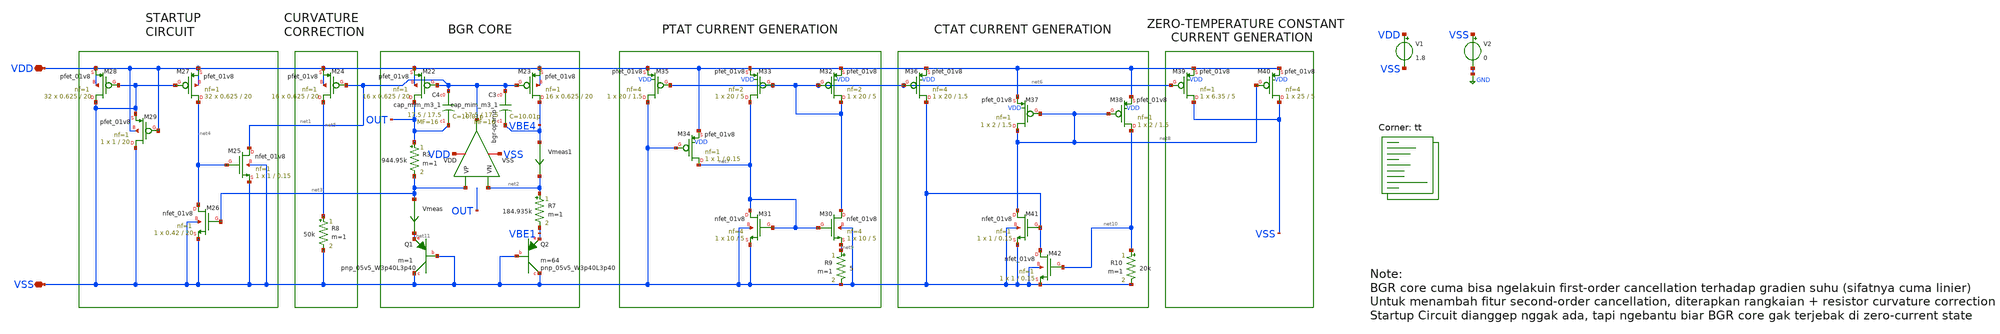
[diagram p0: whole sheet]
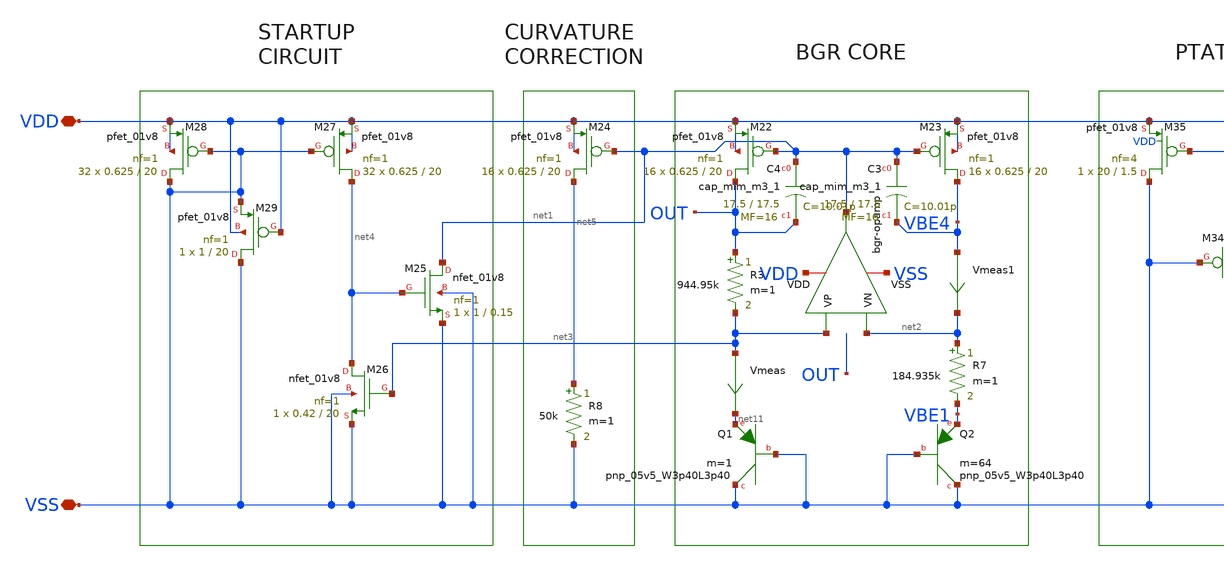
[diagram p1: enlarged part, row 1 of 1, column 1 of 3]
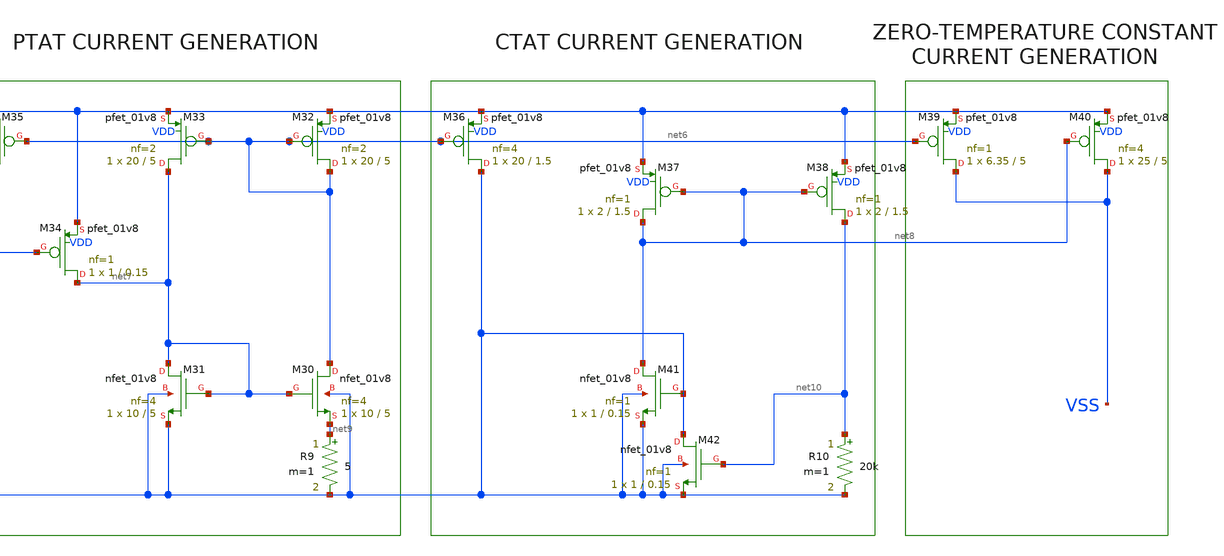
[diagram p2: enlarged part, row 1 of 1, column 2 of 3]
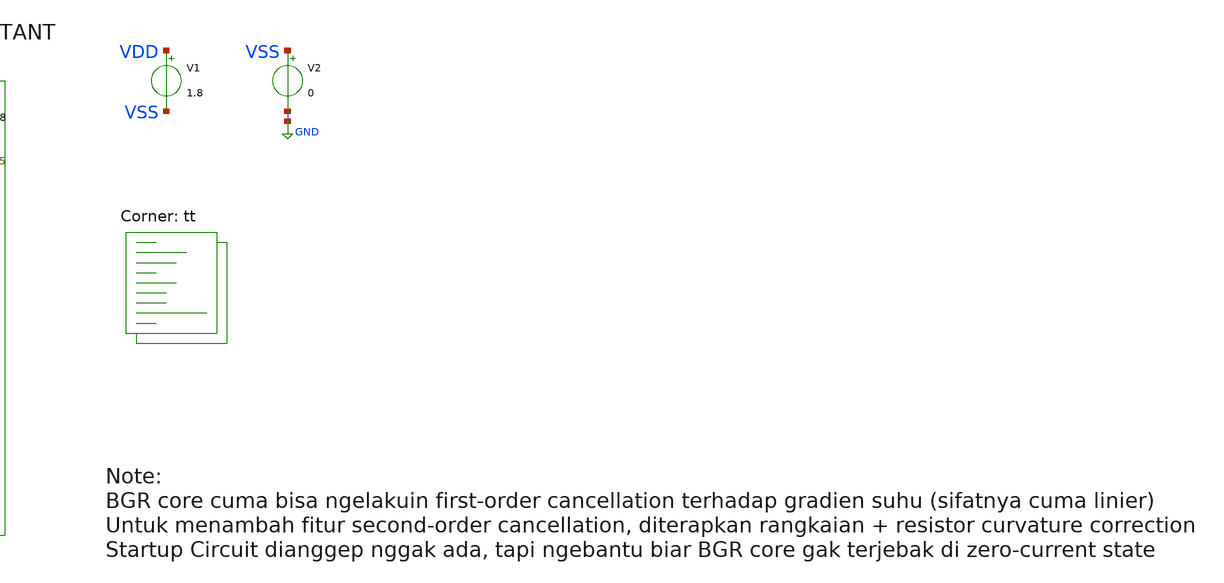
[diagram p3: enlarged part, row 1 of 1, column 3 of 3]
** sch_path: bandgap/bgr2.sch
**.subckt bgr2 VDD VSS
*.iopin VDD
*.iopin VSS
V1 VDD VSS 1.8
V2 VSS GND 0
x1 VDD net1 net3 net2 VSS bgr-opamp
XM22 OUT net1 VDD VDD sky130_fd_pr__pfet_01v8 L=20 W=0.625 nf=1 ad='int((nf+1)/2) * W/nf * 0.29' as='int((nf+2)/2) * W/nf * 0.29'
+ pd='2*int((nf+1)/2) * (W/nf + 0.29)' ps='2*int((nf+2)/2) * (W/nf + 0.29)' nrd='0.29 / W' nrs='0.29 / W'
+ sa=0 sb=0 sd=0 mult=16 m=16
XM23 VBE4 net1 VDD VDD sky130_fd_pr__pfet_01v8 L=20 W=0.625 nf=1 ad='int((nf+1)/2) * W/nf * 0.29' as='int((nf+2)/2) * W/nf * 0.29'
+ pd='2*int((nf+1)/2) * (W/nf + 0.29)' ps='2*int((nf+2)/2) * (W/nf + 0.29)' nrd='0.29 / W' nrs='0.29 / W'
+ sa=0 sb=0 sd=0 mult=16 m=16
R3 OUT net3 944.95k m=1
R7 net2 VBE1 184.935k m=1
XQ1 VSS VSS net11 sky130_fd_pr__pnp_05v5_W3p40L3p40 m=1
XQ2 VSS VSS VBE1 sky130_fd_pr__pnp_05v5_W3p40L3p40 m=64
XM24 net5 net1 VDD VDD sky130_fd_pr__pfet_01v8 L=20 W=0.625 nf=1 ad='int((nf+1)/2) * W/nf * 0.29' as='int((nf+2)/2) * W/nf * 0.29'
+ pd='2*int((nf+1)/2) * (W/nf + 0.29)' ps='2*int((nf+2)/2) * (W/nf + 0.29)' nrd='0.29 / W' nrs='0.29 / W'
+ sa=0 sb=0 sd=0 mult=16 m=16
XM25 net1 net4 VSS VSS sky130_fd_pr__nfet_01v8 L=0.15 W=1 nf=1 ad='int((nf+1)/2) * W/nf * 0.29' as='int((nf+2)/2) * W/nf * 0.29'
+ pd='2*int((nf+1)/2) * (W/nf + 0.29)' ps='2*int((nf+2)/2) * (W/nf + 0.29)' nrd='0.29 / W' nrs='0.29 / W'
+ sa=0 sb=0 sd=0 mult=1 m=1
XM26 net4 net3 VSS VSS sky130_fd_pr__nfet_01v8 L=20 W=0.42 nf=1 ad='int((nf+1)/2) * W/nf * 0.29' as='int((nf+2)/2) * W/nf * 0.29'
+ pd='2*int((nf+1)/2) * (W/nf + 0.29)' ps='2*int((nf+2)/2) * (W/nf + 0.29)' nrd='0.29 / W' nrs='0.29 / W'
+ sa=0 sb=0 sd=0 mult=1 m=1
XM27 net4 VSS VDD VDD sky130_fd_pr__pfet_01v8 L=20 W=0.625 nf=1 ad='int((nf+1)/2) * W/nf * 0.29' as='int((nf+2)/2) * W/nf * 0.29'
+ pd='2*int((nf+1)/2) * (W/nf + 0.29)' ps='2*int((nf+2)/2) * (W/nf + 0.29)' nrd='0.29 / W' nrs='0.29 / W'
+ sa=0 sb=0 sd=0 mult=32 m=32
XM28 VSS VSS VDD VDD sky130_fd_pr__pfet_01v8 L=20 W=0.625 nf=1 ad='int((nf+1)/2) * W/nf * 0.29' as='int((nf+2)/2) * W/nf * 0.29'
+ pd='2*int((nf+1)/2) * (W/nf + 0.29)' ps='2*int((nf+2)/2) * (W/nf + 0.29)' nrd='0.29 / W' nrs='0.29 / W'
+ sa=0 sb=0 sd=0 mult=32 m=32
XM29 VSS VDD VSS VDD sky130_fd_pr__pfet_01v8 L=20 W=1 nf=1 ad='int((nf+1)/2) * W/nf * 0.29' as='int((nf+2)/2) * W/nf * 0.29'
+ pd='2*int((nf+1)/2) * (W/nf + 0.29)' ps='2*int((nf+2)/2) * (W/nf + 0.29)' nrd='0.29 / W' nrs='0.29 / W'
+ sa=0 sb=0 sd=0 mult=1 m=1
R8 net5 VSS 50k m=1
XC3 net1 VBE4 sky130_fd_pr__cap_mim_m3_1 W=17.5 L=17.5 MF=16 m=16
XC4 net1 OUT sky130_fd_pr__cap_mim_m3_1 W=17.5 L=17.5 MF=16 m=16
XM30 net6 net7 net9 VSS sky130_fd_pr__nfet_01v8 L=5 W=10 nf=4 ad='int((nf+1)/2) * W/nf * 0.29' as='int((nf+2)/2) * W/nf * 0.29'
+ pd='2*int((nf+1)/2) * (W/nf + 0.29)' ps='2*int((nf+2)/2) * (W/nf + 0.29)' nrd='0.29 / W' nrs='0.29 / W'
+ sa=0 sb=0 sd=0 mult=1 m=1
XM31 net7 net7 VSS VSS sky130_fd_pr__nfet_01v8 L=5 W=10 nf=4 ad='int((nf+1)/2) * W/nf * 0.29' as='int((nf+2)/2) * W/nf * 0.29'
+ pd='2*int((nf+1)/2) * (W/nf + 0.29)' ps='2*int((nf+2)/2) * (W/nf + 0.29)' nrd='0.29 / W' nrs='0.29 / W'
+ sa=0 sb=0 sd=0 mult=1 m=1
XM32 net6 net6 VDD VDD sky130_fd_pr__pfet_01v8 L=5 W=20 nf=2 ad='int((nf+1)/2) * W/nf * 0.29' as='int((nf+2)/2) * W/nf * 0.29'
+ pd='2*int((nf+1)/2) * (W/nf + 0.29)' ps='2*int((nf+2)/2) * (W/nf + 0.29)' nrd='0.29 / W' nrs='0.29 / W'
+ sa=0 sb=0 sd=0 mult=1 m=1
XM33 net7 net6 VDD VDD sky130_fd_pr__pfet_01v8 L=5 W=20 nf=2 ad='int((nf+1)/2) * W/nf * 0.29' as='int((nf+2)/2) * W/nf * 0.29'
+ pd='2*int((nf+1)/2) * (W/nf + 0.29)' ps='2*int((nf+2)/2) * (W/nf + 0.29)' nrd='0.29 / W' nrs='0.29 / W'
+ sa=0 sb=0 sd=0 mult=1 m=1
XM34 net7 VSS VDD VDD sky130_fd_pr__pfet_01v8 L=0.15 W=1 nf=1 ad='int((nf+1)/2) * W/nf * 0.29' as='int((nf+2)/2) * W/nf * 0.29'
+ pd='2*int((nf+1)/2) * (W/nf + 0.29)' ps='2*int((nf+2)/2) * (W/nf + 0.29)' nrd='0.29 / W' nrs='0.29 / W'
+ sa=0 sb=0 sd=0 mult=1 m=1
XM35 VSS net6 VDD VDD sky130_fd_pr__pfet_01v8 L=1.5 W=20 nf=4 ad='int((nf+1)/2) * W/nf * 0.29' as='int((nf+2)/2) * W/nf * 0.29'
+ pd='2*int((nf+1)/2) * (W/nf + 0.29)' ps='2*int((nf+2)/2) * (W/nf + 0.29)' nrd='0.29 / W' nrs='0.29 / W'
+ sa=0 sb=0 sd=0 mult=1 m=1
XM36 VSS net6 VDD VDD sky130_fd_pr__pfet_01v8 L=1.5 W=20 nf=4 ad='int((nf+1)/2) * W/nf * 0.29' as='int((nf+2)/2) * W/nf * 0.29'
+ pd='2*int((nf+1)/2) * (W/nf + 0.29)' ps='2*int((nf+2)/2) * (W/nf + 0.29)' nrd='0.29 / W' nrs='0.29 / W'
+ sa=0 sb=0 sd=0 mult=1 m=1
XM37 net8 net8 VDD VDD sky130_fd_pr__pfet_01v8 L=1.5 W=2 nf=1 ad='int((nf+1)/2) * W/nf * 0.29' as='int((nf+2)/2) * W/nf * 0.29'
+ pd='2*int((nf+1)/2) * (W/nf + 0.29)' ps='2*int((nf+2)/2) * (W/nf + 0.29)' nrd='0.29 / W' nrs='0.29 / W'
+ sa=0 sb=0 sd=0 mult=1 m=1
XM38 net10 net8 VDD VDD sky130_fd_pr__pfet_01v8 L=1.5 W=2 nf=1 ad='int((nf+1)/2) * W/nf * 0.29' as='int((nf+2)/2) * W/nf * 0.29'
+ pd='2*int((nf+1)/2) * (W/nf + 0.29)' ps='2*int((nf+2)/2) * (W/nf + 0.29)' nrd='0.29 / W' nrs='0.29 / W'
+ sa=0 sb=0 sd=0 mult=1 m=1
XM39 VSS net6 VDD VDD sky130_fd_pr__pfet_01v8 L=5 W=6.35 nf=1 ad='int((nf+1)/2) * W/nf * 0.29' as='int((nf+2)/2) * W/nf * 0.29'
+ pd='2*int((nf+1)/2) * (W/nf + 0.29)' ps='2*int((nf+2)/2) * (W/nf + 0.29)' nrd='0.29 / W' nrs='0.29 / W'
+ sa=0 sb=0 sd=0 mult=1 m=1
XM40 VSS net8 VDD VDD sky130_fd_pr__pfet_01v8 L=5 W=25 nf=4 ad='int((nf+1)/2) * W/nf * 0.29' as='int((nf+2)/2) * W/nf * 0.29'
+ pd='2*int((nf+1)/2) * (W/nf + 0.29)' ps='2*int((nf+2)/2) * (W/nf + 0.29)' nrd='0.29 / W' nrs='0.29 / W'
+ sa=0 sb=0 sd=0 mult=1 m=1
XM41 net8 VSS VSS VSS sky130_fd_pr__nfet_01v8 L=0.15 W=1 nf=1 ad='int((nf+1)/2) * W/nf * 0.29' as='int((nf+2)/2) * W/nf * 0.29'
+ pd='2*int((nf+1)/2) * (W/nf + 0.29)' ps='2*int((nf+2)/2) * (W/nf + 0.29)' nrd='0.29 / W' nrs='0.29 / W'
+ sa=0 sb=0 sd=0 mult=1 m=1
XM42 VSS net10 VSS VSS sky130_fd_pr__nfet_01v8 L=0.15 W=1 nf=1 ad='int((nf+1)/2) * W/nf * 0.29' as='int((nf+2)/2) * W/nf * 0.29'
+ pd='2*int((nf+1)/2) * (W/nf + 0.29)' ps='2*int((nf+2)/2) * (W/nf + 0.29)' nrd='0.29 / W' nrs='0.29 / W'
+ sa=0 sb=0 sd=0 mult=1 m=1
R9 net9 VSS 5 m=1
R10 net10 VSS 20k m=1
Vmeas net3 net11 0
.save i(vmeas)
Vmeas1 VBE4 net2 0
.save i(vmeas1)
**** begin user architecture code
.lib $::SKYWATER_MODELS/sky130.lib.spice tt




.control
 DC temp -40 125 1
 plot OUT2
 let PTAT = 4.94*(VBE2 - VBE1)
 let deltav = OUT - 1.25
 let CC = 4.94*(VBE5)
 let CTAT = VBE1
 let VREF = PTAT + CTAT + CC
 let Verr = VREF - OUT
 let pwr = -i(V1)*1.8

 meas dc vout_max max v(out)
 meas dc vout_min min v(out)
 meas dc line_reg param='(vout_max - vout_min)/0.36'

 Bcorr VREF_CORR 0 V = V(VREF_RAW) - (1.26596064e-2 + (-5.94362766e-7)*(temp-27) +
+ (-5.24694018e-7)*pwr(temp-27,2) + (2.27088537e-9)*pwr(temp-27,3))
 plot V(VREF_CORR)
 plot i(Vmeas) i(Vmeas1)
 plot i(Vmeas1) - i(Vmeas)
 plot pwr
 plot OUT PTAT CTAT
 plot VREF
 plot VERR
 plot VREF - VERR()
 plot deltav
 plot VBIAS

.endc


**** end user architecture code
**.ends

* expanding   symbol:  afe-icdec-teknofest-2026/bandgap/bgr-opamp/bgr-opamp.sym # of pins=5
** sym_path: bandgap/bgr-opamp/bgr-opamp.sym
** sch_path: bandgap/bgr-opamp/bgr-opamp.sch
.subckt bgr-opamp VDD OUT VP VN VSS
*.iopin VSS
*.iopin VDD
*.ipin VP
*.ipin VN
*.opin OUT
XM2 net2 VN net3 VSS sky130_fd_pr__nfet_01v8 L=0.3 W=30 nf=2 ad='int((nf+1)/2) * W/nf * 0.29' as='int((nf+2)/2) * W/nf * 0.29'
+ pd='2*int((nf+1)/2) * (W/nf + 0.29)' ps='2*int((nf+2)/2) * (W/nf + 0.29)' nrd='0.29 / W' nrs='0.29 / W'
+ sa=0 sb=0 sd=0 mult=1 m=1
XM4 net2 net1 VDD VDD sky130_fd_pr__pfet_01v8 L=1.25 W=10.8 nf=4 ad='int((nf+1)/2) * W/nf * 0.29' as='int((nf+2)/2) * W/nf * 0.29'
+ pd='2*int((nf+1)/2) * (W/nf + 0.29)' ps='2*int((nf+2)/2) * (W/nf + 0.29)' nrd='0.29 / W' nrs='0.29 / W'
+ sa=0 sb=0 sd=0 mult=1 m=1
XM3 net1 net1 VDD VDD sky130_fd_pr__pfet_01v8 L=1.25 W=10.8 nf=4 ad='int((nf+1)/2) * W/nf * 0.29' as='int((nf+2)/2) * W/nf * 0.29'
+ pd='2*int((nf+1)/2) * (W/nf + 0.29)' ps='2*int((nf+2)/2) * (W/nf + 0.29)' nrd='0.29 / W' nrs='0.29 / W'
+ sa=0 sb=0 sd=0 mult=1 m=1
XM5 net3 net11 VSS VSS sky130_fd_pr__nfet_01v8 L=1.25 W=3.4 nf=1 ad='int((nf+1)/2) * W/nf * 0.29' as='int((nf+2)/2) * W/nf * 0.29'
+ pd='2*int((nf+1)/2) * (W/nf + 0.29)' ps='2*int((nf+2)/2) * (W/nf + 0.29)' nrd='0.29 / W' nrs='0.29 / W'
+ sa=0 sb=0 sd=0 mult=1 m=1
XM9 net4 net5 net12 VSS sky130_fd_pr__nfet_01v8 L=1.25 W=13.6 nf=1 ad='int((nf+1)/2) * W/nf * 0.29' as='int((nf+2)/2) * W/nf * 0.29'
+ pd='2*int((nf+1)/2) * (W/nf + 0.29)' ps='2*int((nf+2)/2) * (W/nf + 0.29)' nrd='0.29 / W' nrs='0.29 / W'
+ sa=0 sb=0 sd=0 mult=1 m=1
XM8 net4 net4 VDD VDD sky130_fd_pr__pfet_01v8 L=1.25 W=10.8 nf=4 ad='int((nf+1)/2) * W/nf * 0.29' as='int((nf+2)/2) * W/nf * 0.29'
+ pd='2*int((nf+1)/2) * (W/nf + 0.29)' ps='2*int((nf+2)/2) * (W/nf + 0.29)' nrd='0.29 / W' nrs='0.29 / W'
+ sa=0 sb=0 sd=0 mult=1 m=1
XM11 net5 net4 VDD VDD sky130_fd_pr__pfet_01v8 L=1.25 W=10.8 nf=4 ad='int((nf+1)/2) * W/nf * 0.29' as='int((nf+2)/2) * W/nf * 0.29'
+ pd='2*int((nf+1)/2) * (W/nf + 0.29)' ps='2*int((nf+2)/2) * (W/nf + 0.29)' nrd='0.29 / W' nrs='0.29 / W'
+ sa=0 sb=0 sd=0 mult=1 m=1
XM10 net5 net5 net6 net6 sky130_fd_pr__nfet_01v8 L=1.25 W=3.4 nf=1 ad='int((nf+1)/2) * W/nf * 0.29' as='int((nf+2)/2) * W/nf * 0.29'
+ pd='2*int((nf+1)/2) * (W/nf + 0.29)' ps='2*int((nf+2)/2) * (W/nf + 0.29)' nrd='0.29 / W' nrs='0.29 / W'
+ sa=0 sb=0 sd=0 mult=1 m=1
XM6 OUT net2 VDD VDD sky130_fd_pr__pfet_01v8 L=1.25 W=100 nf=32 ad='int((nf+1)/2) * W/nf * 0.29' as='int((nf+2)/2) * W/nf * 0.29'
+ pd='2*int((nf+1)/2) * (W/nf + 0.29)' ps='2*int((nf+2)/2) * (W/nf + 0.29)' nrd='0.29 / W' nrs='0.29 / W'
+ sa=0 sb=0 sd=0 mult=1 m=1
XM7 OUT net11 VSS VSS sky130_fd_pr__nfet_01v8 L=1.25 W=14 nf=4 ad='int((nf+1)/2) * W/nf * 0.29' as='int((nf+2)/2) * W/nf * 0.29'
+ pd='2*int((nf+1)/2) * (W/nf + 0.29)' ps='2*int((nf+2)/2) * (W/nf + 0.29)' nrd='0.29 / W' nrs='0.29 / W'
+ sa=0 sb=0 sd=0 mult=1 m=1
XC2 OUT net2 sky130_fd_pr__cap_mim_m3_1 W=25 L=25 MF=32 m=32
XR2 net7 net12 VSS sky130_fd_pr__res_high_po_1p41 L=3.235 mult=1 m=1
XR3 net9 net7 VSS sky130_fd_pr__res_high_po_1p41 L=3.235 mult=1 m=1
XR4 net8 net9 VSS sky130_fd_pr__res_high_po_1p41 L=3.235 mult=1 m=1
XR5 net10 net8 VSS sky130_fd_pr__res_high_po_1p41 L=3.235 mult=1 m=1
XR6 VSS net10 VSS sky130_fd_pr__res_high_po_1p41 L=3.235 mult=1 m=1
XM13 net11 net4 VDD VDD sky130_fd_pr__pfet_01v8 L=1.25 W=10.8 nf=4 ad='int((nf+1)/2) * W/nf * 0.29' as='int((nf+2)/2) * W/nf * 0.29'
+ pd='2*int((nf+1)/2) * (W/nf + 0.29)' ps='2*int((nf+2)/2) * (W/nf + 0.29)' nrd='0.29 / W' nrs='0.29 / W'
+ sa=0 sb=0 sd=0 mult=1 m=1
XM14 net11 net11 VSS VSS sky130_fd_pr__nfet_01v8 L=1.25 W=6.8 nf=1 ad='int((nf+1)/2) * W/nf * 0.29' as='int((nf+2)/2) * W/nf * 0.29'
+ pd='2*int((nf+1)/2) * (W/nf + 0.29)' ps='2*int((nf+2)/2) * (W/nf + 0.29)' nrd='0.29 / W' nrs='0.29 / W'
+ sa=0 sb=0 sd=0 mult=1 m=1
XM15 net6 net6 VSS VSS sky130_fd_pr__nfet_01v8 L=1.25 W=3.4 nf=1 ad='int((nf+1)/2) * W/nf * 0.29' as='int((nf+2)/2) * W/nf * 0.29'
+ pd='2*int((nf+1)/2) * (W/nf + 0.29)' ps='2*int((nf+2)/2) * (W/nf + 0.29)' nrd='0.29 / W' nrs='0.29 / W'
+ sa=0 sb=0 sd=0 mult=1 m=1
XM12 net5 net4 net4 VSS sky130_fd_pr__pfet_01v8 L=0.15 W=0.85 nf=1 ad='int((nf+1)/2) * W/nf * 0.29' as='int((nf+2)/2) * W/nf * 0.29'
+ pd='2*int((nf+1)/2) * (W/nf + 0.29)' ps='2*int((nf+2)/2) * (W/nf + 0.29)' nrd='0.29 / W' nrs='0.29 / W'
+ sa=0 sb=0 sd=0 mult=1 m=1
XM16 net1 VP net3 VSS sky130_fd_pr__nfet_01v8 L=0.3 W=30 nf=2 ad='int((nf+1)/2) * W/nf * 0.29' as='int((nf+2)/2) * W/nf * 0.29'
+ pd='2*int((nf+1)/2) * (W/nf + 0.29)' ps='2*int((nf+2)/2) * (W/nf + 0.29)' nrd='0.29 / W' nrs='0.29 / W'
+ sa=0 sb=0 sd=0 mult=1 m=1
.ends

.GLOBAL GND
.end
